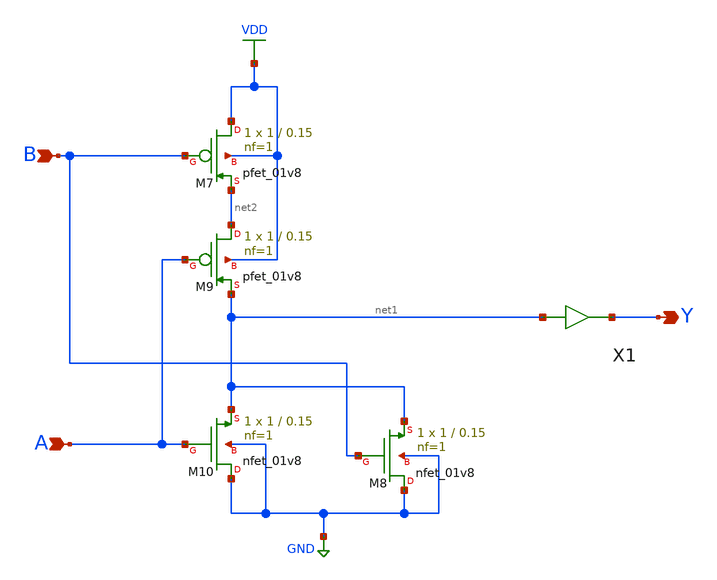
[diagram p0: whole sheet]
** sch_path: gates/OR2.sch
**.subckt OR2 A B Y
*.ipin A
*.ipin B
*.opin Y
XM7 VDD B net2 VDD sky130_fd_pr__pfet_01v8 L=0.15 W=1 nf=1 ad='int((nf+1)/2) * W/nf * 0.29' as='int((nf+2)/2) * W/nf * 0.29'
+ pd='2*int((nf+1)/2) * (W/nf + 0.29)' ps='2*int((nf+2)/2) * (W/nf + 0.29)' nrd='0.29 / W' nrs='0.29 / W'
+ sa=0 sb=0 sd=0 mult=1 m=1
XM8 GND B net1 GND sky130_fd_pr__nfet_01v8 L=0.15 W=1 nf=1 ad='int((nf+1)/2) * W/nf * 0.29' as='int((nf+2)/2) * W/nf * 0.29'
+ pd='2*int((nf+1)/2) * (W/nf + 0.29)' ps='2*int((nf+2)/2) * (W/nf + 0.29)' nrd='0.29 / W' nrs='0.29 / W'
+ sa=0 sb=0 sd=0 mult=1 m=1
XM9 net2 A net1 VDD sky130_fd_pr__pfet_01v8 L=0.15 W=1 nf=1 ad='int((nf+1)/2) * W/nf * 0.29' as='int((nf+2)/2) * W/nf * 0.29'
+ pd='2*int((nf+1)/2) * (W/nf + 0.29)' ps='2*int((nf+2)/2) * (W/nf + 0.29)' nrd='0.29 / W' nrs='0.29 / W'
+ sa=0 sb=0 sd=0 mult=1 m=1
XM10 GND A net1 GND sky130_fd_pr__nfet_01v8 L=0.15 W=1 nf=1 ad='int((nf+1)/2) * W/nf * 0.29' as='int((nf+2)/2) * W/nf * 0.29'
+ pd='2*int((nf+1)/2) * (W/nf + 0.29)' ps='2*int((nf+2)/2) * (W/nf + 0.29)' nrd='0.29 / W' nrs='0.29 / W'
+ sa=0 sb=0 sd=0 mult=1 m=1
X1 net1 Y inv_vtc
**.ends

* expanding   symbol:  /home/apn/test_xschem_sky130/inv_vtc.sym # of pins=2
** sym_path: gates/inv_vtc.sym
** sch_path: gates/inv_vtc.sch
.subckt inv_vtc A Y
*.ipin A
*.opin Y
XM1 Y A VDD VDD sky130_fd_pr__pfet_01v8 L=0.15 W=2 nf=1 ad='int((nf+1)/2) * W/nf * 0.29' as='int((nf+2)/2) * W/nf * 0.29'
+ pd='2*int((nf+1)/2) * (W/nf + 0.29)' ps='2*int((nf+2)/2) * (W/nf + 0.29)' nrd='0.29 / W' nrs='0.29 / W'
+ sa=0 sb=0 sd=0 mult=1 m=1
XM2 Y A GND GND sky130_fd_pr__nfet_01v8 L=0.15 W=1 nf=1 ad='int((nf+1)/2) * W/nf * 0.29' as='int((nf+2)/2) * W/nf * 0.29'
+ pd='2*int((nf+1)/2) * (W/nf + 0.29)' ps='2*int((nf+2)/2) * (W/nf + 0.29)' nrd='0.29 / W' nrs='0.29 / W'
+ sa=0 sb=0 sd=0 mult=1 m=1
.ends

.GLOBAL VDD
.GLOBAL GND
.end
